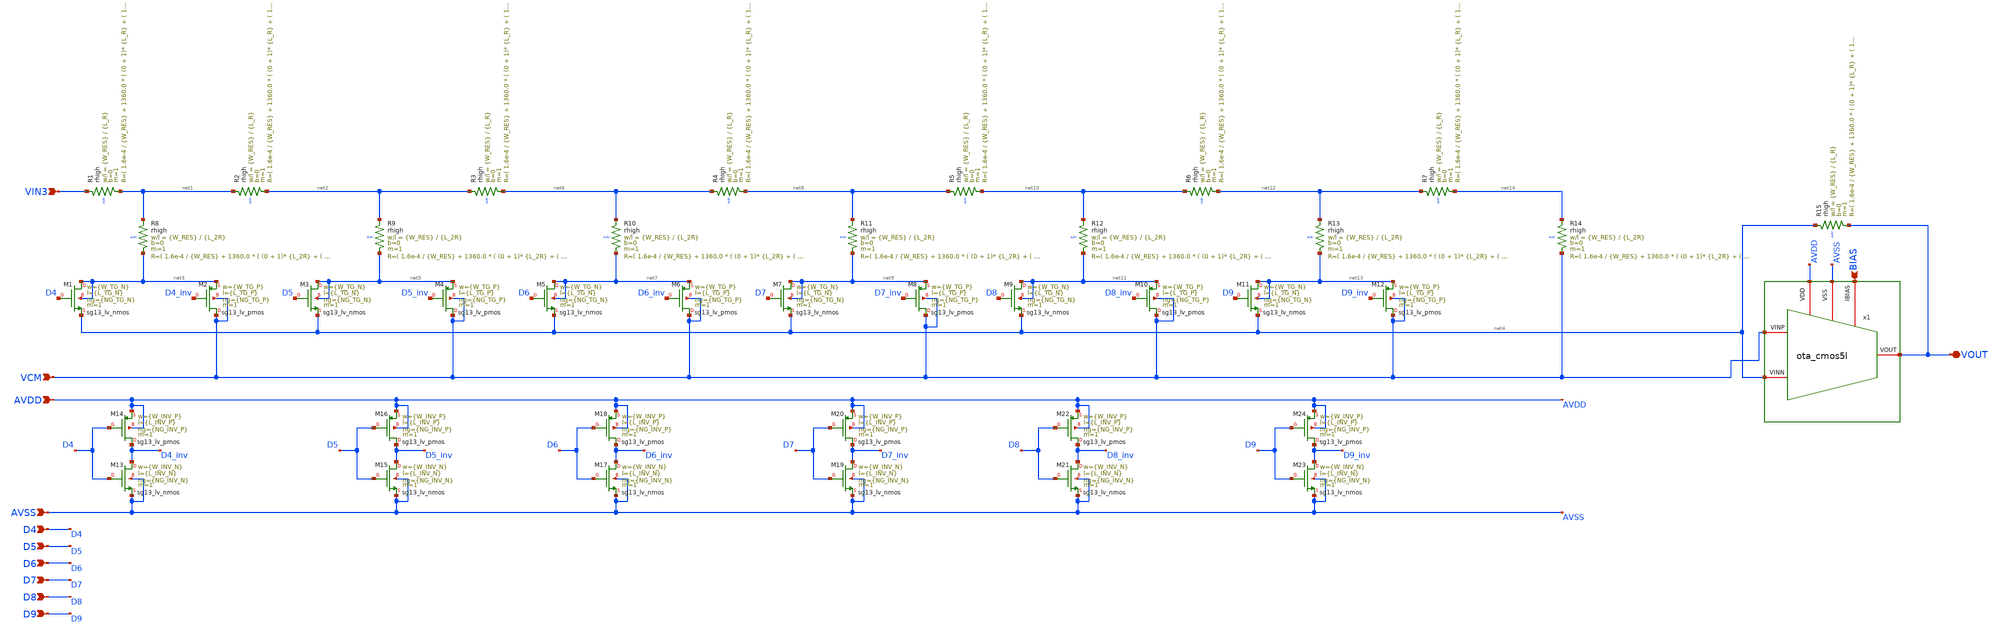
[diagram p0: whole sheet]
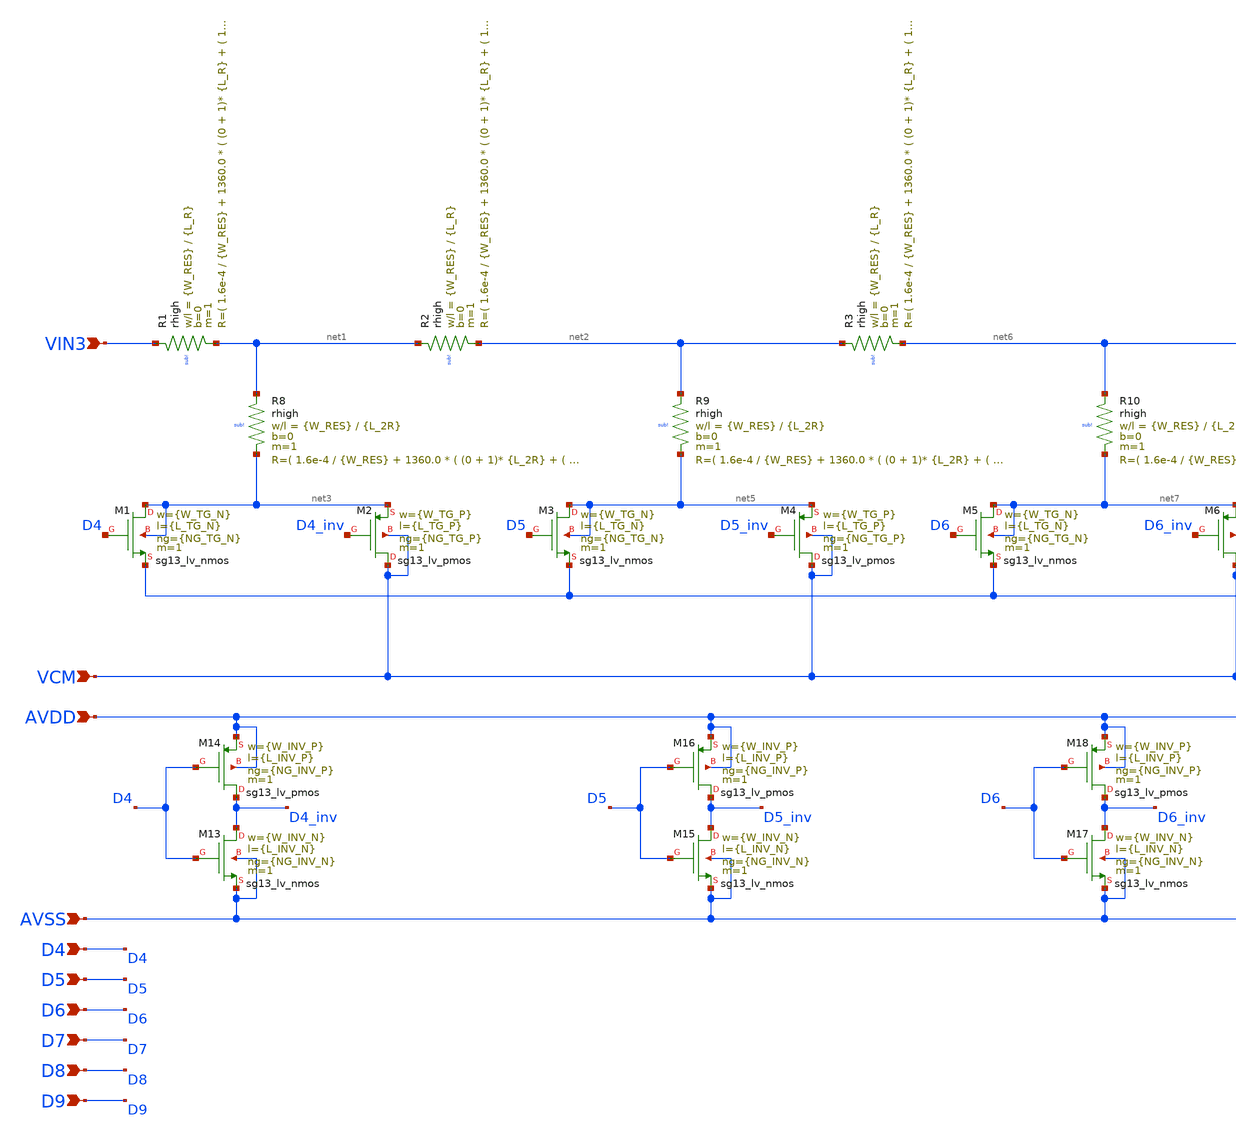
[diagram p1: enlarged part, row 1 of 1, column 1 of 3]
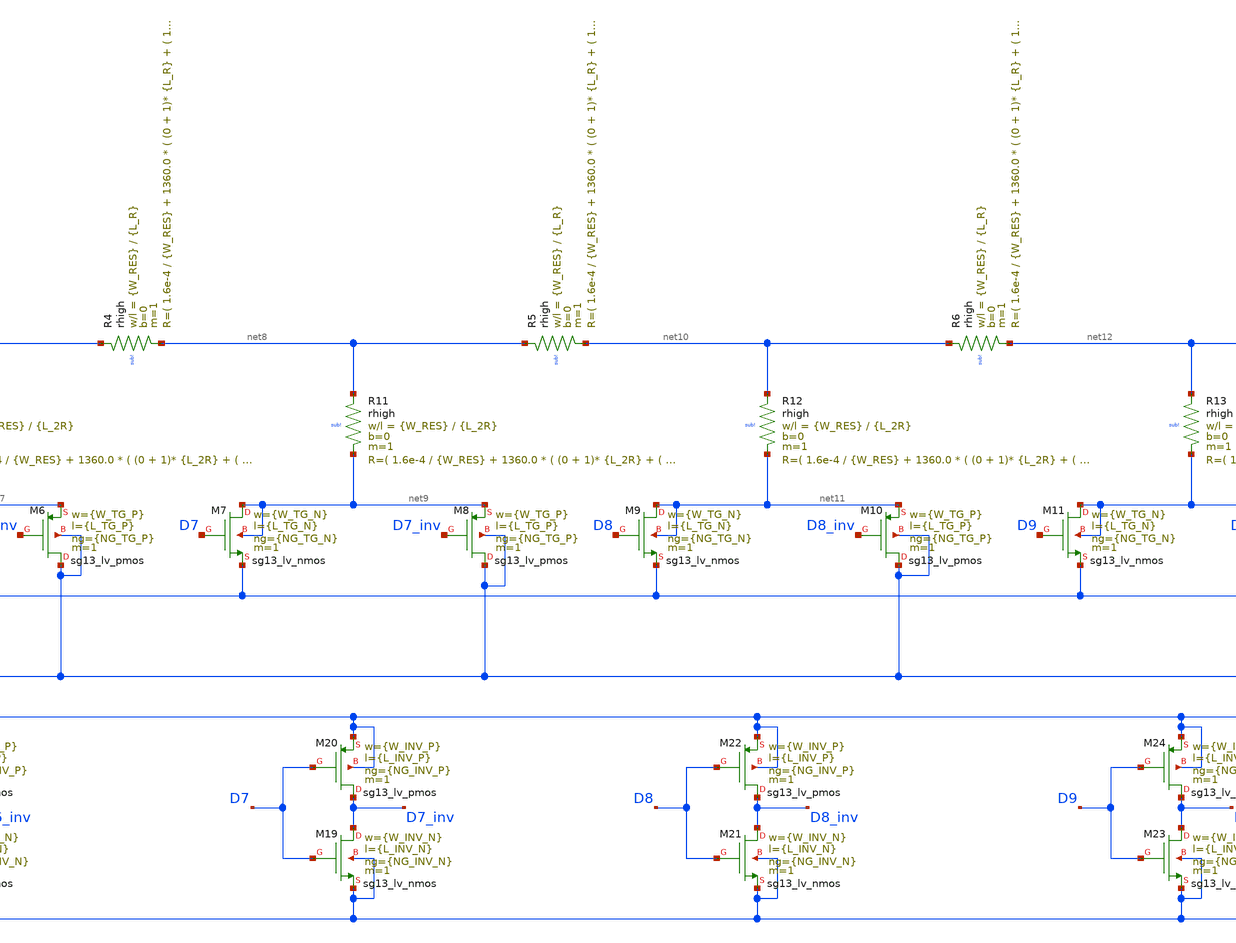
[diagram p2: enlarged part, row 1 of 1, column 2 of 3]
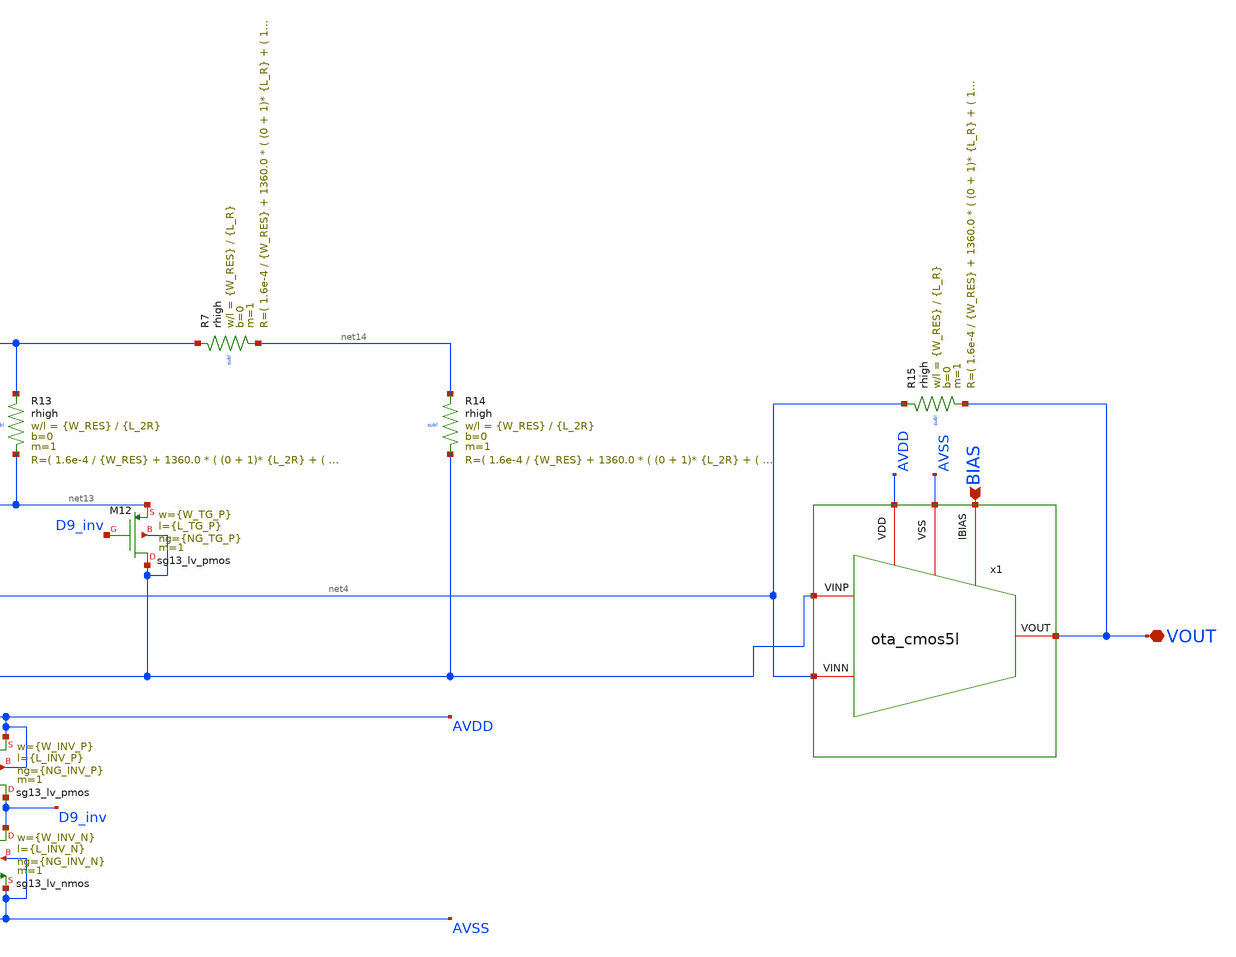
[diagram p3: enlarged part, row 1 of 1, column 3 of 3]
** sch_path: archives/fine_gain/fine_gain.sch
**.subckt fine_gain VIN3 VCM D4 D5 D6 D7 D8 D9 BIAS VOUT AVDD AVSS
*.ipin VIN3
*.ipin VCM
*.ipin D4
*.ipin D5
*.ipin D6
*.ipin D7
*.ipin D8
*.ipin D9
*.ipin BIAS
*.iopin VOUT
*.ipin AVDD
*.ipin AVSS
XR1 VIN3 net1 sub! rhigh w={W_RES} l={L_R} m=1 b=0 mm_ok=1
XM1 net3 D4 net4 net3 sg13_lv_nmos w={W_TG_N} l={L_TG_N} ng={NG_TG_N} m=1 mm_ok=1
XM2 VCM D4_inv net3 VCM sg13_lv_pmos w={W_TG_P} l={L_TG_P} ng={NG_TG_P} m=1 mm_ok=1
XR2 net1 net2 sub! rhigh w={W_RES} l={L_R} m=1 b=0 mm_ok=1
XR8 net1 net3 sub! rhigh w={W_RES} l={L_2R} m=1 b=0 mm_ok=1
XR9 net2 net5 sub! rhigh w={W_RES} l={L_2R} m=1 b=0 mm_ok=1
XR15 net4 VOUT sub! rhigh w={W_RES} l={L_R} m=1 b=0 mm_ok=1
XM3 net5 D5 net4 net5 sg13_lv_nmos w={W_TG_N} l={L_TG_N} ng={NG_TG_N} m=1 mm_ok=1
XM4 VCM D5_inv net5 VCM sg13_lv_pmos w={W_TG_P} l={L_TG_P} ng={NG_TG_P} m=1 mm_ok=1
XR3 net2 net6 sub! rhigh w={W_RES} l={L_R} m=1 b=0 mm_ok=1
XR4 net6 net8 sub! rhigh w={W_RES} l={L_R} m=1 b=0 mm_ok=1
XR5 net8 net10 sub! rhigh w={W_RES} l={L_R} m=1 b=0 mm_ok=1
XR6 net10 net12 sub! rhigh w={W_RES} l={L_R} m=1 b=0 mm_ok=1
XR7 net12 net14 sub! rhigh w={W_RES} l={L_R} m=1 b=0 mm_ok=1
XR10 net6 net7 sub! rhigh w={W_RES} l={L_2R} m=1 b=0 mm_ok=1
XM5 net7 D6 net4 net7 sg13_lv_nmos w={W_TG_N} l={L_TG_N} ng={NG_TG_N} m=1 mm_ok=1
XM6 VCM D6_inv net7 VCM sg13_lv_pmos w={W_TG_P} l={L_TG_P} ng={NG_TG_P} m=1 mm_ok=1
XR11 net8 net9 sub! rhigh w={W_RES} l={L_2R} m=1 b=0 mm_ok=1
XM7 net9 D7 net4 net9 sg13_lv_nmos w={W_TG_N} l={L_TG_N} ng={NG_TG_N} m=1 mm_ok=1
XM8 VCM D7_inv net9 VCM sg13_lv_pmos w={W_TG_P} l={L_TG_P} ng={NG_TG_P} m=1 mm_ok=1
XR12 net10 net11 sub! rhigh w={W_RES} l={L_2R} m=1 b=0 mm_ok=1
XM9 net11 D8 net4 net11 sg13_lv_nmos w={W_TG_N} l={L_TG_N} ng={NG_TG_N} m=1 mm_ok=1
XM10 VCM D8_inv net11 VCM sg13_lv_pmos w={W_TG_P} l={L_TG_P} ng={NG_TG_P} m=1 mm_ok=1
XR13 net12 net13 sub! rhigh w={W_RES} l={L_2R} m=1 b=0 mm_ok=1
XM11 net13 D9 net4 net13 sg13_lv_nmos w={W_TG_N} l={L_TG_N} ng={NG_TG_N} m=1 mm_ok=1
XM12 VCM D9_inv net13 VCM sg13_lv_pmos w={W_TG_P} l={L_TG_P} ng={NG_TG_P} m=1 mm_ok=1
XR14 net14 VCM sub! rhigh w={W_RES} l={L_2R} m=1 b=0 mm_ok=1
XM13 D4_inv D4 AVSS AVSS sg13_lv_nmos w={W_INV_N} l={L_INV_N} ng={NG_INV_N} m=1 mm_ok=1
XM14 D4_inv D4 AVDD AVDD sg13_lv_pmos w={W_INV_P} l={L_INV_P} ng={NG_INV_P} m=1 mm_ok=1
XM15 D5_inv D5 AVSS AVSS sg13_lv_nmos w={W_INV_N} l={L_INV_N} ng={NG_INV_N} m=1 mm_ok=1
XM16 D5_inv D5 AVDD AVDD sg13_lv_pmos w={W_INV_P} l={L_INV_P} ng={NG_INV_P} m=1 mm_ok=1
XM17 D6_inv D6 AVSS AVSS sg13_lv_nmos w={W_INV_N} l={L_INV_N} ng={NG_INV_N} m=1 mm_ok=1
XM18 D6_inv D6 AVDD AVDD sg13_lv_pmos w={W_INV_P} l={L_INV_P} ng={NG_INV_P} m=1 mm_ok=1
XM19 D7_inv D7 AVSS AVSS sg13_lv_nmos w={W_INV_N} l={L_INV_N} ng={NG_INV_N} m=1 mm_ok=1
XM20 D7_inv D7 AVDD AVDD sg13_lv_pmos w={W_INV_P} l={L_INV_P} ng={NG_INV_P} m=1 mm_ok=1
XM21 D8_inv D8 AVSS AVSS sg13_lv_nmos w={W_INV_N} l={L_INV_N} ng={NG_INV_N} m=1 mm_ok=1
XM22 D8_inv D8 AVDD AVDD sg13_lv_pmos w={W_INV_P} l={L_INV_P} ng={NG_INV_P} m=1 mm_ok=1
XM23 D9_inv D9 AVSS AVSS sg13_lv_nmos w={W_INV_N} l={L_INV_N} ng={NG_INV_N} m=1 mm_ok=1
XM24 D9_inv D9 AVDD AVDD sg13_lv_pmos w={W_INV_P} l={L_INV_P} ng={NG_INV_P} m=1 mm_ok=1
x1 AVSS BIAS AVDD net4 VCM VOUT ota_cmos5l
**.ends

* expanding   symbol:
*+  /foss/designs/chipalooza/Programmable-Instrumentation-Amplifier-IP/xschem/ota_cmos5l/ota_cmos5l.sym # of pins=6
** sym_path: xschem/output_buffer/ota_cmos5l.sym
** sch_path: xschem/output_buffer/ota_cmos5l.sch
.subckt ota_cmos5l VSS IBIAS VDD VINN VINP VOUT
*.iopin IBIAS
*.iopin VDD
*.iopin VSS
*.iopin VOUT
*.iopin VINP
*.iopin VINN
XM6 IBIAS IBIAS VDD VDD sg13_lv_pmos w={wbias} l={lbias} ng=1 m={m6} mm_ok=1
XM7 net1 IBIAS VDD VDD sg13_lv_pmos w={wbias} l={lbias} ng=1 m={m7} mm_ok=1
XM8 VOUT IBIAS VDD VDD sg13_lv_pmos w={wbias} l={lbias} ng=1 m={m8} mm_ok=1
XM1 net2 VINN net1 VDD sg13_lv_pmos w={winpair} l={linpair} ng=1 m=1 mm_ok=1
XM2 net3 VINP net1 VDD sg13_lv_pmos w={winpair} l={linpair} ng=1 m=1 mm_ok=1
XM3 net2 net2 VSS VSS sg13_lv_nmos w={wload} l={lload} ng=1 m=1 mm_ok=1
XM4 net3 net2 VSS VSS sg13_lv_nmos w={wload} l={lload} ng=1 m=1 mm_ok=1
XM5 VOUT net3 VSS VSS sg13_lv_nmos w={wcs} l={lcs} ng=1 m=1 mm_ok=1
XR1 net3 net4 VSS rhigh w=0.5e-6 l=1.95e-6 m=1 b=0 mm_ok=1
.save v(vinp)
.save v(vinn)
.save v(vout)
XC2 VOUT net4 cap_cmomi w=15e-6 l=15e-6 mmin=1 mmax=4 feed=double subblock=0 m=5 mm_ok=1
**** begin user architecture code


.param temp=27
.param lbias=0.15u wbias=0.15u
.param m6=1 m7=4 m8=8
.param linpair=3u winpair=20u
.param lload=5u wload=10u
.param lcs=3u wcs=20u
.param Cc=2p



**** end user architecture code
XC1 VOUT net4 cap_cmomi w=15e-6 l=15e-6 mmin=1 mmax=4 feed=double subblock=0 m=4 mm_ok=1
.ends

.end
